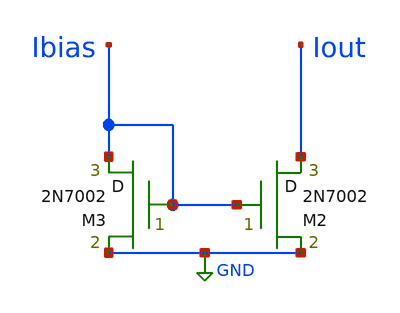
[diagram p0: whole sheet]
** sch_path: ISSCC25/submitted_notebooks/MicroNina/sch/CurrentMirror.sch
**.subckt CurrentMirror
M2 Iout Ibias GND M2N7002 m=1
M3 Ibias Ibias GND M2N7002 m=1
**.ends
.GLOBAL GND
.end
